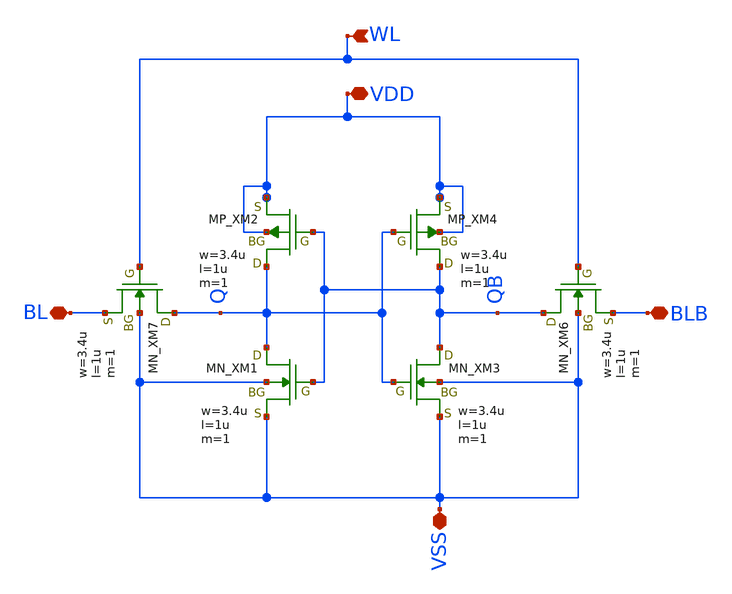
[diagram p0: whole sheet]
** sch_path: member_project/SRAM/PenguinEino/sram512/schematics/sram512_bitcell.sch
**.subckt sram512_bitcell VDD BLB BL WL VSS
*.iopin VDD
*.iopin BLB
*.iopin BL
*.ipin WL
*.iopin VSS
XXM1 Q QB VSS VSS NMOS w=3.4u l=1u nrd=0 nrs=0 m=1
XXM2 Q QB VDD VDD PMOS w=3.4u l=1u nrd=0 nrs=0 m=1
XXM3 QB Q VSS VSS NMOS w=3.4u l=1u nrd=0 nrs=0 m=1
XXM4 QB Q VDD VDD PMOS w=3.4u l=1u nrd=0 nrs=0 m=1
XXM7 Q WL BL VSS NMOS w=3.4u l=1u nrd=0 nrs=0 m=1
XXM6 QB WL BLB VSS NMOS w=3.4u l=1u nrd=0 nrs=0 m=1
**.ends
.end
